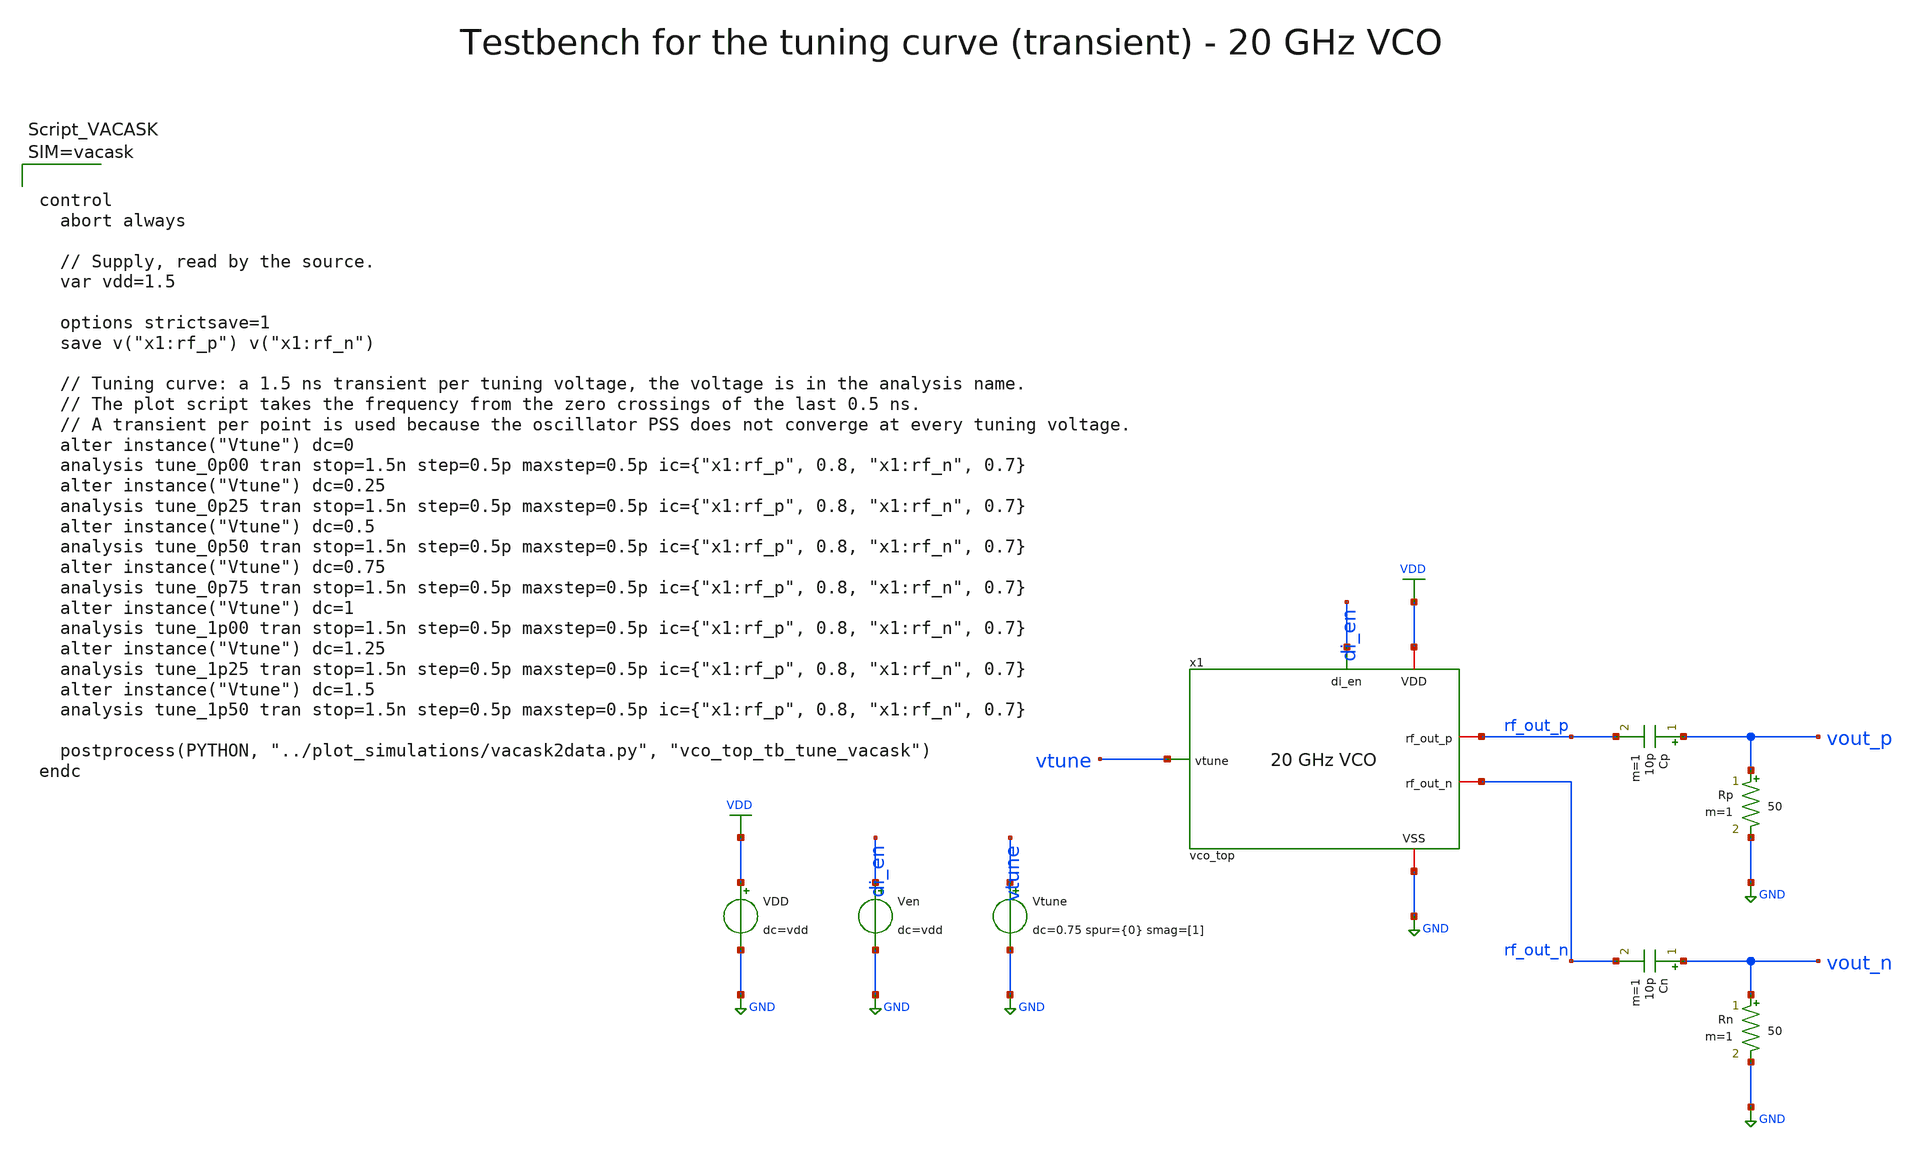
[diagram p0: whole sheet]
** sch_path: macros/vco/testbenches/xschem/vco_top_tb_tune_vacask.sch
**.subckt vco_top_tb_tune_vacask
x1 di_en VDD GND vtune rf_out_p rf_out_n vco_top
Cp vout_p rf_out_p 10p m=1
Rp vout_p GND 50 m=1
Cn vout_n rf_out_n 10p m=1
Rn vout_n GND 50 m=1
VDD VDD GND dc=vdd
Ven di_en GND dc=vdd
Vtune vtune GND dc=0.75 spur={0} smag=[1]
**** begin user architecture code






**** end user architecture code
**.ends
.GLOBAL VDD
.GLOBAL GND
.end
